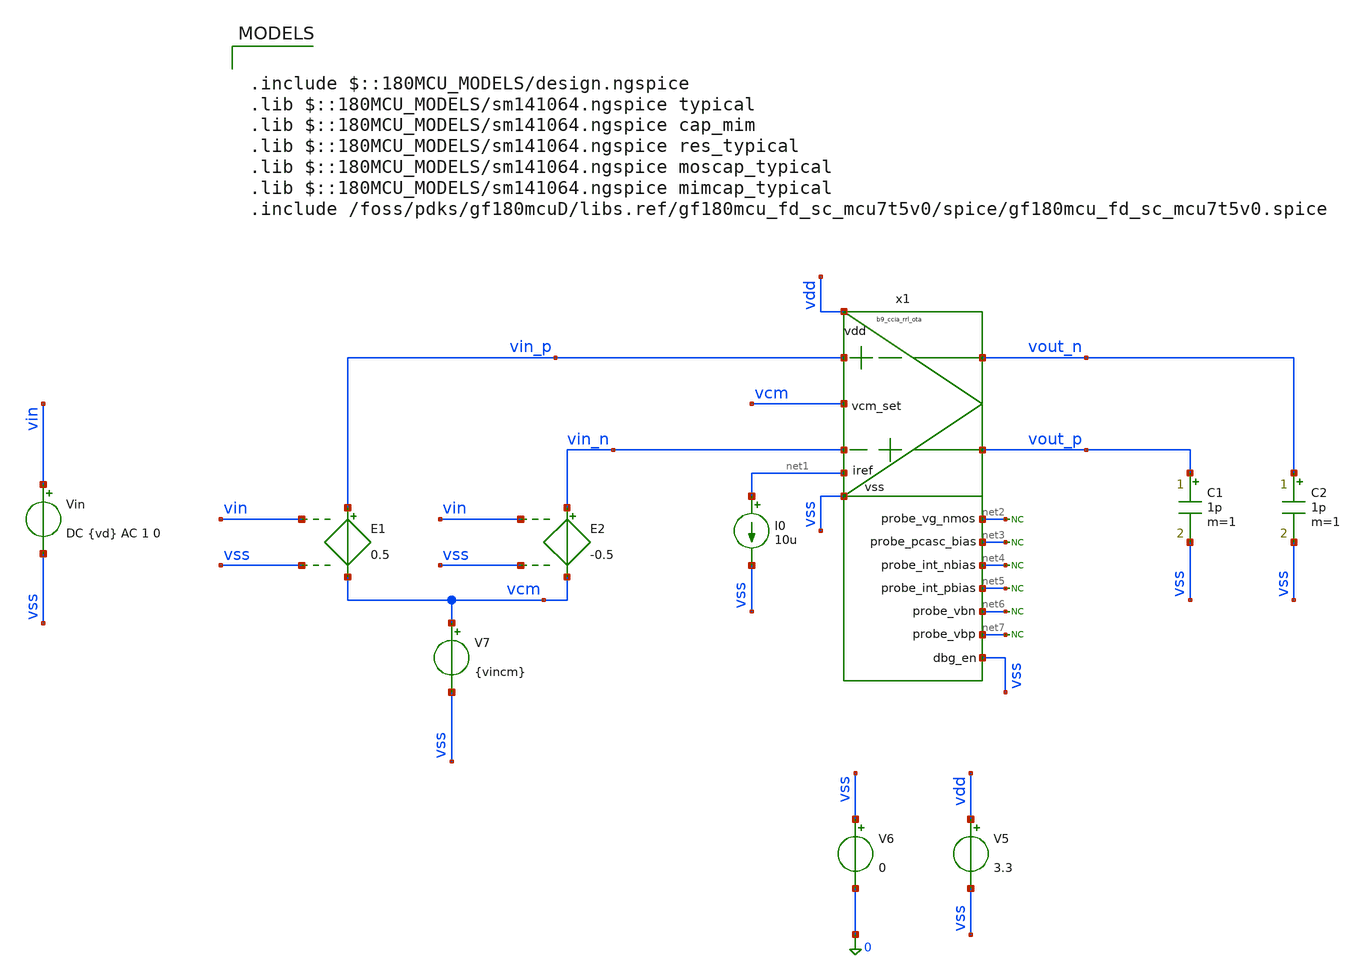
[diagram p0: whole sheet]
** sch_path: xschem/ccia_rrl_ota/b9_ccia_rrl_ota_tb_basic.sch
**.subckt b9_ccia_rrl_ota_tb_basic
x1 vin_p net6 vin_n net7 net3 vout_p vout_n net4 vdd net5 vss net2 vss vcm net1 b9_ccia_rrl_ota
I0 net1 vss 10u
* noconn #net2
* noconn #net3
* noconn #net4
* noconn #net5
* noconn #net6
* noconn #net7
C1 vout_p vss 1p m=1
C2 vout_n vss 1p m=1
V7 vcm vss {vincm}
E1 vin_p vcm vin vss 0.5
E2 vin_n vcm vin vss -0.5
Vin vin vss DC {vd} AC 1 0
V5 vdd vss 3.3
V6 vss 0 0
**** begin user architecture code

.include $::180MCU_MODELS/design.ngspice
.lib $::180MCU_MODELS/sm141064.ngspice typical
.lib $::180MCU_MODELS/sm141064.ngspice cap_mim
.lib $::180MCU_MODELS/sm141064.ngspice res_typical
.lib $::180MCU_MODELS/sm141064.ngspice moscap_typical
.lib $::180MCU_MODELS/sm141064.ngspice mimcap_typical
.include /foss/pdks/gf180mcuD/libs.ref/gf180mcu_fd_sc_mcu7t5v0/spice/gf180mcu_fd_sc_mcu7t5v0.spice


.param vincm=1
.param voutcm=0.8
.param vd=0
.control
save all
save @m.x1.x1.xm2.m0[id] @m.x1.x1.xm2.m0[gm] @m.x1.x1.xm2.m0[gds] @m.x1.x1.xm2.m0[cdb]
+ @m.x1.x1.xm2.m0[cgs] @m.x1.x1.xm2.m0[csb] @m.x1.x1.xm2.m0[cgd]
save @m.x1.x1.xm3.m0[id] @m.x1.x1.xm3.m0[gm] @m.x1.x1.xm3.m0[gds] @m.x1.x1.xm3.m0[cdb]
+ @m.x1.x1.xm3.m0[cgs] @m.x1.x1.xm3.m0[csb] @m.x1.x1.xm3.m0[cgd]
save @m.x1.x4.xm4.m0[id] @m.x1.x4.xm4.m0[gm] @m.x1.x4.xm4.m0[gds] @m.x1.x4.xm4.m0[cdb]
+ @m.x1.x4.xm4.m0[cgs] @m.x1.x4.xm4.m0[csb] @m.x1.x4.xm4.m0[cgd]
save @m.x1.x4.xm16.m0[id] @m.x1.x4.xm16.m0[gm] @m.x1.x4.xm16.m0[gds] @m.x1.x4.xm16.m0[cdb]
+ @m.x1.x4.xm16.m0[cgs] @m.x1.x4.xm16.m0[csb] @m.x1.x4.xm16.m0[cgd]
save @m.x1.x4.xm17.m0[id] @m.x1.x4.xm17.m0[gm] @m.x1.x4.xm17.m0[gds] @m.x1.x4.xm17.m0[cdb]
+ @m.x1.x4.xm17.m0[cgs] @m.x1.x4.xm17.m0[csb] @m.x1.x4.xm17.m0[cgd]
save @m.x1.x4.xm18.m0[id] @m.x1.x4.xm18.m0[gm] @m.x1.x4.xm18.m0[gds] @m.x1.x4.xm18.m0[cdb]
+ @m.x1.x4.xm18.m0[cgs] @m.x1.x4.xm18.m0[csb] @m.x1.x4.xm18.m0[cgd]
save @m.x1.x2.xm10.m0[id] @m.x1.x2.xm10.m0[gm] @m.x1.x2.xm10.m0[gds] @m.x1.x2.xm10.m0[cdb]
+ @m.x1.x2.xm10.m0[cgs] @m.x1.x2.xm10.m0[csb] @m.x1.x2.xm10.m0[cgd]
save @m.x1.x2.xm11.m0[id] @m.x1.x2.xm11.m0[gm] @m.x1.x2.xm11.m0[gds] @m.x1.x2.xm11.m0[cdb]
+ @m.x1.x2.xm11.m0[cgs] @m.x1.x2.xm11.m0[csb] @m.x1.x2.xm11.m0[cgd]
save @m.x1.x2.xm7.m0[id] @m.x1.x2.xm7.m0[gm] @m.x1.x2.xm7.m0[gds] @m.x1.x2.xm7.m0[cdb]
+ @m.x1.x2.xm7.m0[cgs] @m.x1.x2.xm7.m0[csb] @m.x1.x2.xm7.m0[cgd]
save @m.x1.x2.xm8.m0[id] @m.x1.x2.xm8.m0[gm] @m.x1.x2.xm8.m0[gds] @m.x1.x2.xm8.m0[cdb]
+ @m.x1.x2.xm8.m0[cgs] @m.x1.x2.xm8.m0[csb] @m.x1.x2.xm8.m0[cgd]
save @m.x1.x5.xm12.m0[id] @m.x1.x5.xm12.m0[gm] @m.x1.x5.xm12.m0[gds] @m.x1.x5.xm12.m0[cdb]
+ @m.x1.x5.xm12.m0[cgs] @m.x1.x5.xm12.m0[csb] @m.x1.x5.xm12.m0[cgd]
save @m.x1.x5.xm13.m0[id] @m.x1.x5.xm13.m0[gm] @m.x1.x5.xm13.m0[gds] @m.x1.x5.xm13.m0[cdb]
+ @m.x1.x5.xm13.m0[cgs] @m.x1.x5.xm13.m0[csb] @m.x1.x5.xm13.m0[cgd]
save @m.x1.x5.xm19.m0[id] @m.x1.x5.xm19.m0[gm] @m.x1.x5.xm19.m0[gds] @m.x1.x5.xm19.m0[cdb]
+ @m.x1.x5.xm19.m0[cgs] @m.x1.x5.xm19.m0[csb] @m.x1.x5.xm19.m0[cgd]
save @m.x1.x5.xm22.m0[id] @m.x1.x5.xm22.m0[gm] @m.x1.x5.xm22.m0[gds] @m.x1.x5.xm22.m0[cdb]
+ @m.x1.x5.xm22.m0[cgs] @m.x1.x5.xm22.m0[csb] @m.x1.x5.xm22.m0[cgd]
save @m.x1.x5.xm25.m0[id] @m.x1.x5.xm25.m0[gm] @m.x1.x5.xm25.m0[gds] @m.x1.x5.xm25.m0[cdb]
+ @m.x1.x5.xm25.m0[cgs] @m.x1.x5.xm25.m0[csb] @m.x1.x5.xm25.m0[cgd]
save @m.x1.x5.xm26.m0[id] @m.x1.x5.xm26.m0[gm] @m.x1.x5.xm26.m0[gds] @m.x1.x5.xm26.m0[cdb]
+ @m.x1.x5.xm26.m0[cgs] @m.x1.x5.xm26.m0[csb] @m.x1.x5.xm26.m0[cgd]
save @m.x1.x5.xm27.m0[id] @m.x1.x5.xm27.m0[gm] @m.x1.x5.xm27.m0[gds] @m.x1.x5.xm27.m0[cdb]
+ @m.x1.x5.xm27.m0[cgs] @m.x1.x5.xm27.m0[csb] @m.x1.x5.xm27.m0[cgd]
save @m.x1.x5.xm28.m0[id] @m.x1.x5.xm28.m0[gm] @m.x1.x5.xm28.m0[gds] @m.x1.x5.xm28.m0[cdb]
+ @m.x1.x5.xm28.m0[cgs] @m.x1.x5.xm28.m0[csb] @m.x1.x5.xm28.m0[cgd]
save @m.x1.x5.xm20.m0[id] @m.x1.x5.xm20.m0[gm] @m.x1.x5.xm20.m0[gds] @m.x1.x5.xm20.m0[cdb]
+ @m.x1.x5.xm20.m0[cgs] @m.x1.x5.xm20.m0[csb] @m.x1.x5.xm20.m0[cgd]
save @m.x1.x5.xm21.m0[id] @m.x1.x5.xm21.m0[gm] @m.x1.x5.xm21.m0[gds] @m.x1.x5.xm21.m0[cdb]
+ @m.x1.x5.xm21.m0[cgs] @m.x1.x5.xm21.m0[csb] @m.x1.x5.xm21.m0[cgd]
save @m.x1.x5.xm23.m0[id] @m.x1.x5.xm23.m0[gm] @m.x1.x5.xm23.m0[gds] @m.x1.x5.xm23.m0[cdb]
+ @m.x1.x5.xm23.m0[cgs] @m.x1.x5.xm23.m0[csb] @m.x1.x5.xm23.m0[cgd]
save @m.x1.x3.xm1.m0[id] @m.x1.x3.xm1.m0[gm] @m.x1.x3.xm1.m0[gds] @m.x1.x3.xm1.m0[cdb]
+ @m.x1.x3.xm1.m0[cgs] @m.x1.x3.xm1.m0[csb] @m.x1.x3.xm1.m0[cgd]
save @m.x1.x3.xm5.m0[id] @m.x1.x3.xm5.m0[gm] @m.x1.x3.xm5.m0[gds] @m.x1.x3.xm5.m0[cdb]
+ @m.x1.x3.xm5.m0[cgs] @m.x1.x3.xm5.m0[csb] @m.x1.x3.xm5.m0[cgd]
save @m.x1.x3.xm15.m0[id] @m.x1.x3.xm15.m0[gm] @m.x1.x3.xm15.m0[gds] @m.x1.x3.xm15.m0[cdb]
+ @m.x1.x3.xm15.m0[cgs] @m.x1.x3.xm15.m0[csb] @m.x1.x3.xm15.m0[cgd]
save @m.x1.x3.xm9.m0[id] @m.x1.x3.xm9.m0[gm] @m.x1.x3.xm9.m0[gds] @m.x1.x3.xm9.m0[cdb]
+ @m.x1.x3.xm9.m0[cgs] @m.x1.x3.xm9.m0[csb] @m.x1.x3.xm9.m0[cgd]
save @m.x1.x3.xm6.m0[id] @m.x1.x3.xm6.m0[gm] @m.x1.x3.xm6.m0[gds] @m.x1.x3.xm6.m0[cdb]
+ @m.x1.x3.xm6.m0[cgs] @m.x1.x3.xm6.m0[csb] @m.x1.x3.xm6.m0[cgd]
save @m.x1.x3.xm14.m0[id] @m.x1.x3.xm14.m0[gm] @m.x1.x3.xm14.m0[gds] @m.x1.x3.xm14.m0[cdb]
+ @m.x1.x3.xm14.m0[cgs] @m.x1.x3.xm14.m0[csb] @m.x1.x3.xm14.m0[cgd]
save @m.x1.x7.x1.xm1.m0[id] @m.x1.x7.x1.xm1.m0[gm] @m.x1.x7.x1.xm1.m0[gds] @m.x1.x7.x1.xm1.m0[cdb]
+ @m.x1.x7.x1.xm1.m0[cgs] @m.x1.x7.x1.xm1.m0[csb] @m.x1.x7.x1.xm1.m0[cgd]
save @m.x1.x7.x1.xm2.m0[id] @m.x1.x7.x1.xm2.m0[gm] @m.x1.x7.x1.xm2.m0[gds] @m.x1.x7.x1.xm2.m0[cdb]
+ @m.x1.x7.x1.xm2.m0[cgs] @m.x1.x7.x1.xm2.m0[csb] @m.x1.x7.x1.xm2.m0[cgd]
save @m.x1.x7.xm1.m0[id] @m.x1.x7.xm1.m0[gm] @m.x1.x7.xm1.m0[gds] @m.x1.x7.xm1.m0[cdb]
+ @m.x1.x7.xm1.m0[cgs] @m.x1.x7.xm1.m0[csb] @m.x1.x7.xm1.m0[cgd]
save @m.x1.x8.x1.xm1.m0[id] @m.x1.x8.x1.xm1.m0[gm] @m.x1.x8.x1.xm1.m0[gds] @m.x1.x8.x1.xm1.m0[cdb]
+ @m.x1.x8.x1.xm1.m0[cgs] @m.x1.x8.x1.xm1.m0[csb] @m.x1.x8.x1.xm1.m0[cgd]
save @m.x1.x8.x1.xm2.m0[id] @m.x1.x8.x1.xm2.m0[gm] @m.x1.x8.x1.xm2.m0[gds] @m.x1.x8.x1.xm2.m0[cdb]
+ @m.x1.x8.x1.xm2.m0[cgs] @m.x1.x8.x1.xm2.m0[csb] @m.x1.x8.x1.xm2.m0[cgd]
save @m.x1.x8.xm1.m0[id] @m.x1.x8.xm1.m0[gm] @m.x1.x8.xm1.m0[gds] @m.x1.x8.xm1.m0[cdb]
+ @m.x1.x8.xm1.m0[cgs] @m.x1.x8.xm1.m0[csb] @m.x1.x8.xm1.m0[cgd]
save @m.x1.x9.x1.xm1.m0[id] @m.x1.x9.x1.xm1.m0[gm] @m.x1.x9.x1.xm1.m0[gds] @m.x1.x9.x1.xm1.m0[cdb]
+ @m.x1.x9.x1.xm1.m0[cgs] @m.x1.x9.x1.xm1.m0[csb] @m.x1.x9.x1.xm1.m0[cgd]
save @m.x1.x9.x1.xm2.m0[id] @m.x1.x9.x1.xm2.m0[gm] @m.x1.x9.x1.xm2.m0[gds] @m.x1.x9.x1.xm2.m0[cdb]
+ @m.x1.x9.x1.xm2.m0[cgs] @m.x1.x9.x1.xm2.m0[csb] @m.x1.x9.x1.xm2.m0[cgd]
save @m.x1.x9.xm1.m0[id] @m.x1.x9.xm1.m0[gm] @m.x1.x9.xm1.m0[gds] @m.x1.x9.xm1.m0[cdb]
+ @m.x1.x9.xm1.m0[cgs] @m.x1.x9.xm1.m0[csb] @m.x1.x9.xm1.m0[cgd]
save @m.x1.x10.x1.xm1.m0[id] @m.x1.x10.x1.xm1.m0[gm] @m.x1.x10.x1.xm1.m0[gds]
+ @m.x1.x10.x1.xm1.m0[cdb] @m.x1.x10.x1.xm1.m0[cgs] @m.x1.x10.x1.xm1.m0[csb] @m.x1.x10.x1.xm1.m0[cgd]
save @m.x1.x10.x1.xm2.m0[id] @m.x1.x10.x1.xm2.m0[gm] @m.x1.x10.x1.xm2.m0[gds]
+ @m.x1.x10.x1.xm2.m0[cdb] @m.x1.x10.x1.xm2.m0[cgs] @m.x1.x10.x1.xm2.m0[csb] @m.x1.x10.x1.xm2.m0[cgd]
save @m.x1.x10.xm1.m0[id] @m.x1.x10.xm1.m0[gm] @m.x1.x10.xm1.m0[gds] @m.x1.x10.xm1.m0[cdb]
+ @m.x1.x10.xm1.m0[cgs] @m.x1.x10.xm1.m0[csb] @m.x1.x10.xm1.m0[cgd]
save @m.x1.x11.x1.xm1.m0[id] @m.x1.x11.x1.xm1.m0[gm] @m.x1.x11.x1.xm1.m0[gds]
+ @m.x1.x11.x1.xm1.m0[cdb] @m.x1.x11.x1.xm1.m0[cgs] @m.x1.x11.x1.xm1.m0[csb] @m.x1.x11.x1.xm1.m0[cgd]
save @m.x1.x11.x1.xm2.m0[id] @m.x1.x11.x1.xm2.m0[gm] @m.x1.x11.x1.xm2.m0[gds]
+ @m.x1.x11.x1.xm2.m0[cdb] @m.x1.x11.x1.xm2.m0[cgs] @m.x1.x11.x1.xm2.m0[csb] @m.x1.x11.x1.xm2.m0[cgd]
save @m.x1.x11.xm1.m0[id] @m.x1.x11.xm1.m0[gm] @m.x1.x11.xm1.m0[gds] @m.x1.x11.xm1.m0[cdb]
+ @m.x1.x11.xm1.m0[cgs] @m.x1.x11.xm1.m0[csb] @m.x1.x11.xm1.m0[cgd]
save @m.x1.x12.x1.xm1.m0[id] @m.x1.x12.x1.xm1.m0[gm] @m.x1.x12.x1.xm1.m0[gds]
+ @m.x1.x12.x1.xm1.m0[cdb] @m.x1.x12.x1.xm1.m0[cgs] @m.x1.x12.x1.xm1.m0[csb] @m.x1.x12.x1.xm1.m0[cgd]
save @m.x1.x12.x1.xm2.m0[id] @m.x1.x12.x1.xm2.m0[gm] @m.x1.x12.x1.xm2.m0[gds]
+ @m.x1.x12.x1.xm2.m0[cdb] @m.x1.x12.x1.xm2.m0[cgs] @m.x1.x12.x1.xm2.m0[csb] @m.x1.x12.x1.xm2.m0[cgd]
save @m.x1.x12.xm1.m0[id] @m.x1.x12.xm1.m0[gm] @m.x1.x12.xm1.m0[gds] @m.x1.x12.xm1.m0[cdb]
+ @m.x1.x12.xm1.m0[cgs] @m.x1.x12.xm1.m0[csb] @m.x1.x12.xm1.m0[cgd]
save @m.x1.x6.m0[id] @m.x1.x6.m0[gm] @m.x1.x6.m0[gds] @m.x1.x6.m0[cdb] @m.x1.x6.m0[cgs]
+ @m.x1.x6.m0[csb] @m.x1.x6.m0[cgd]

op
write ota_op.raw all
ac dec 100 1 10G
write ota_ac.raw all
.endc


**** end user architecture code
**.ends
.end
